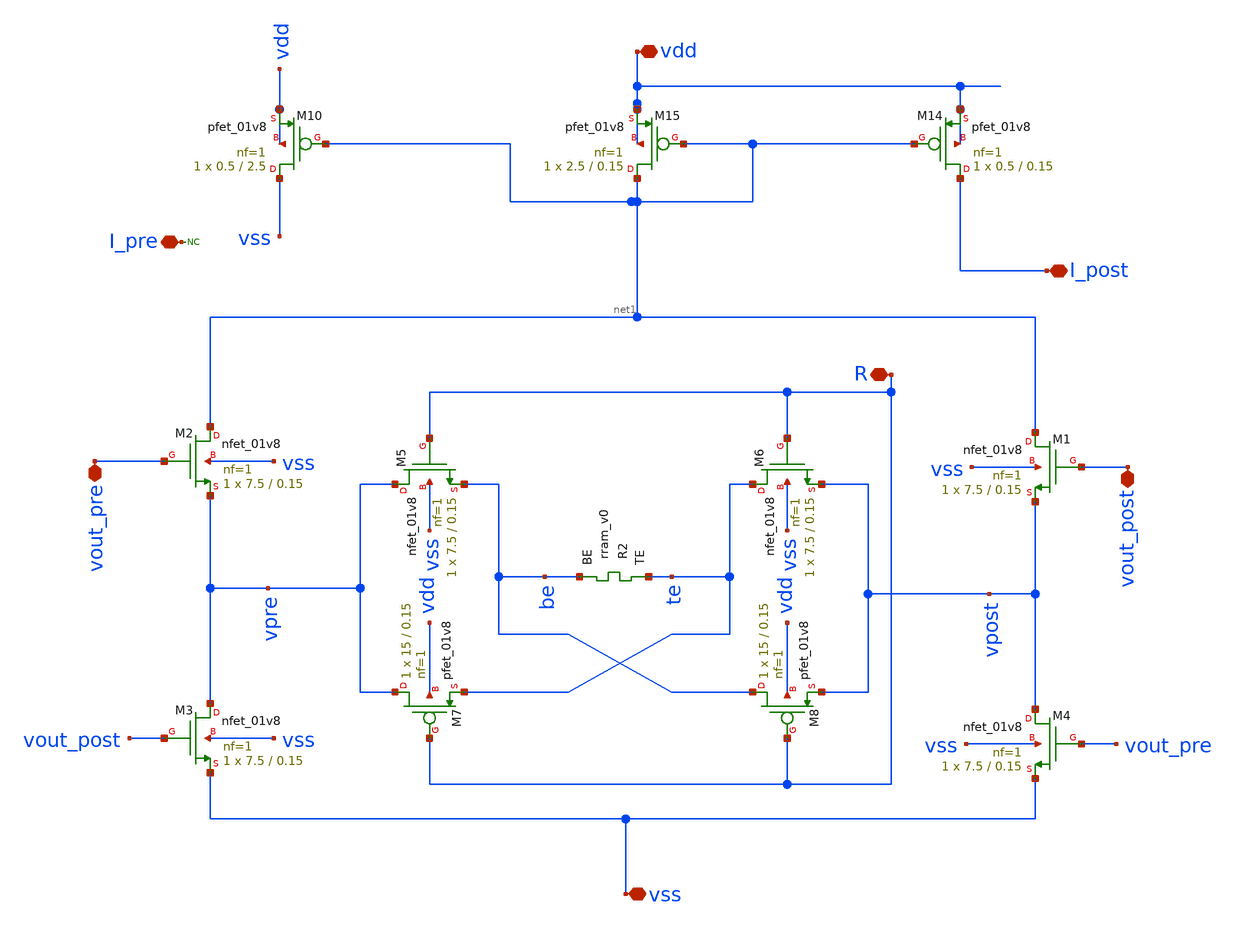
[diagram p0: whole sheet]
** sch_path: Synapse/rstdp_mirror.sch
**.subckt rstdp_mirror vdd vss R vout_post vout_pre I_post I_pre
*.iopin vdd
*.iopin vss
*.iopin R
*.iopin vout_post
*.iopin vout_pre
*.iopin I_post
*.iopin I_pre
XM2 net1 vout_pre vpre vss sky130_fd_pr__nfet_01v8 L=0.15 W=7.5 nf=1 ad='int((nf+1)/2) * W/nf * 0.29'
+ as='int((nf+2)/2) * W/nf * 0.29' pd='2*int((nf+1)/2) * (W/nf + 0.29)' ps='2*int((nf+2)/2) * (W/nf + 0.29)'
+ nrd='0.29 / W' nrs='0.29 / W' sa=0 sb=0 sd=0 mult=1 m=1
XM3 vpre vout_post vss vss sky130_fd_pr__nfet_01v8 L=0.15 W=7.5 nf=1 ad='int((nf+1)/2) * W/nf * 0.29'
+ as='int((nf+2)/2) * W/nf * 0.29' pd='2*int((nf+1)/2) * (W/nf + 0.29)' ps='2*int((nf+2)/2) * (W/nf + 0.29)'
+ nrd='0.29 / W' nrs='0.29 / W' sa=0 sb=0 sd=0 mult=1 m=1
XM1 net1 vout_post vpost vss sky130_fd_pr__nfet_01v8 L=0.15 W=7.5 nf=1 ad='int((nf+1)/2) * W/nf * 0.29'
+ as='int((nf+2)/2) * W/nf * 0.29' pd='2*int((nf+1)/2) * (W/nf + 0.29)' ps='2*int((nf+2)/2) * (W/nf + 0.29)'
+ nrd='0.29 / W' nrs='0.29 / W' sa=0 sb=0 sd=0 mult=1 m=1
XM4 vpost vout_pre vss vss sky130_fd_pr__nfet_01v8 L=0.15 W=7.5 nf=1 ad='int((nf+1)/2) * W/nf * 0.29'
+ as='int((nf+2)/2) * W/nf * 0.29' pd='2*int((nf+1)/2) * (W/nf + 0.29)' ps='2*int((nf+2)/2) * (W/nf + 0.29)'
+ nrd='0.29 / W' nrs='0.29 / W' sa=0 sb=0 sd=0 mult=1 m=1
XM10 vss net1 vdd vdd sky130_fd_pr__pfet_01v8 L=2.5 W=0.5 nf=1 ad='int((nf+1)/2) * W/nf * 0.29' as='int((nf+2)/2) * W/nf * 0.29'
+ pd='2*int((nf+1)/2) * (W/nf + 0.29)' ps='2*int((nf+2)/2) * (W/nf + 0.29)' nrd='0.29 / W' nrs='0.29 / W'
+ sa=0 sb=0 sd=0 mult=1 m=1
XR2 te be rram_v0
XM5 vpre R be vss sky130_fd_pr__nfet_01v8 L=0.15 W=7.5 nf=1 ad='int((nf+1)/2) * W/nf * 0.29' as='int((nf+2)/2) * W/nf * 0.29'
+ pd='2*int((nf+1)/2) * (W/nf + 0.29)' ps='2*int((nf+2)/2) * (W/nf + 0.29)' nrd='0.29 / W' nrs='0.29 / W'
+ sa=0 sb=0 sd=0 mult=1 m=1
XM6 te R vpost vss sky130_fd_pr__nfet_01v8 L=0.15 W=7.5 nf=1 ad='int((nf+1)/2) * W/nf * 0.29' as='int((nf+2)/2) * W/nf * 0.29'
+ pd='2*int((nf+1)/2) * (W/nf + 0.29)' ps='2*int((nf+2)/2) * (W/nf + 0.29)' nrd='0.29 / W' nrs='0.29 / W'
+ sa=0 sb=0 sd=0 mult=1 m=1
XM7 vpre R te vdd sky130_fd_pr__pfet_01v8 L=0.15 W=15 nf=1 ad='int((nf+1)/2) * W/nf * 0.29' as='int((nf+2)/2) * W/nf * 0.29'
+ pd='2*int((nf+1)/2) * (W/nf + 0.29)' ps='2*int((nf+2)/2) * (W/nf + 0.29)' nrd='0.29 / W' nrs='0.29 / W'
+ sa=0 sb=0 sd=0 mult=1 m=1
XM8 be R vpost vdd sky130_fd_pr__pfet_01v8 L=0.15 W=15 nf=1 ad='int((nf+1)/2) * W/nf * 0.29' as='int((nf+2)/2) * W/nf * 0.29'
+ pd='2*int((nf+1)/2) * (W/nf + 0.29)' ps='2*int((nf+2)/2) * (W/nf + 0.29)' nrd='0.29 / W' nrs='0.29 / W'
+ sa=0 sb=0 sd=0 mult=1 m=1
XM14 I_post net1 vdd vdd sky130_fd_pr__pfet_01v8 L=0.15 W=0.5 nf=1 ad='int((nf+1)/2) * W/nf * 0.29' as='int((nf+2)/2) * W/nf * 0.29'
+ pd='2*int((nf+1)/2) * (W/nf + 0.29)' ps='2*int((nf+2)/2) * (W/nf + 0.29)' nrd='0.29 / W' nrs='0.29 / W'
+ sa=0 sb=0 sd=0 mult=1 m=1
XM15 net1 net1 vdd vdd sky130_fd_pr__pfet_01v8 L=0.15 W=2.5 nf=1 ad='int((nf+1)/2) * W/nf * 0.29' as='int((nf+2)/2) * W/nf * 0.29'
+ pd='2*int((nf+1)/2) * (W/nf + 0.29)' ps='2*int((nf+2)/2) * (W/nf + 0.29)' nrd='0.29 / W' nrs='0.29 / W'
+ sa=0 sb=0 sd=0 mult=1 m=1
* noconn I_pre
**.ends
.end
